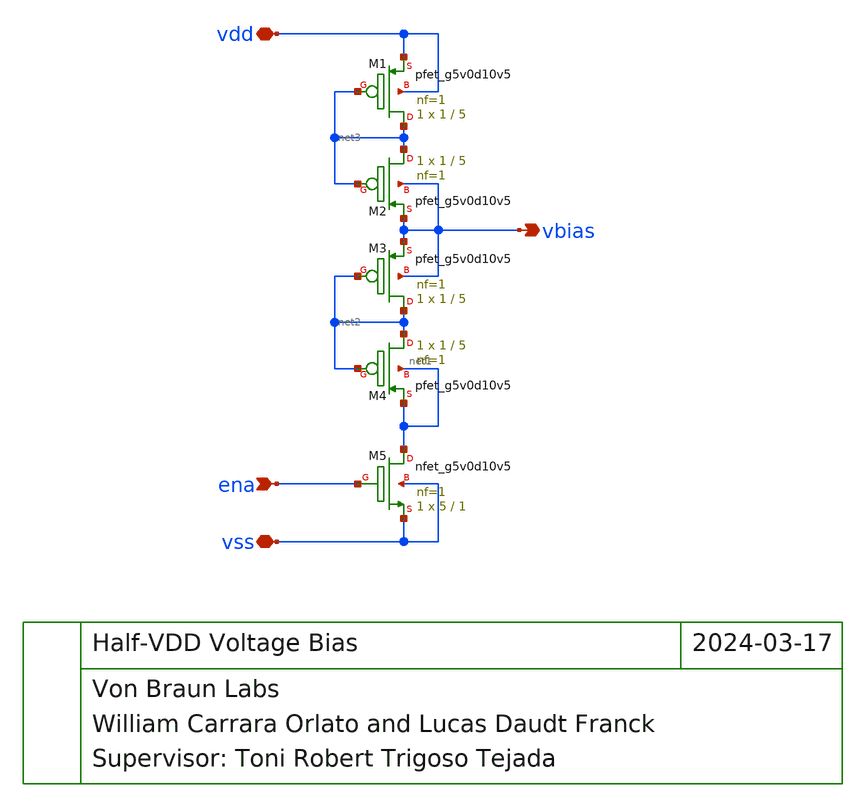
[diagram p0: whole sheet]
** sch_path: xschem_final/halfvdd_vbias.sch
**.subckt halfvdd_vbias ena vss vdd vbias
*.ipin ena
*.iopin vss
*.iopin vdd
*.opin vbias
XM1 net3 net3 vdd vdd sky130_fd_pr__pfet_g5v0d10v5 L=5 W=1 nf=1 ad='int((nf+1)/2) * W/nf * 0.29' as='int((nf+2)/2) * W/nf * 0.29'
+ pd='2*int((nf+1)/2) * (W/nf + 0.29)' ps='2*int((nf+2)/2) * (W/nf + 0.29)' nrd='0.29 / W' nrs='0.29 / W'
+ sa=0 sb=0 sd=0 mult=1 m=1
XM2 net3 net3 vbias vbias sky130_fd_pr__pfet_g5v0d10v5 L=5 W=1 nf=1 ad='int((nf+1)/2) * W/nf * 0.29'
+ as='int((nf+2)/2) * W/nf * 0.29' pd='2*int((nf+1)/2) * (W/nf + 0.29)' ps='2*int((nf+2)/2) * (W/nf + 0.29)'
+ nrd='0.29 / W' nrs='0.29 / W' sa=0 sb=0 sd=0 mult=1 m=1
XM3 net2 net2 vbias vbias sky130_fd_pr__pfet_g5v0d10v5 L=5 W=1 nf=1 ad='int((nf+1)/2) * W/nf * 0.29'
+ as='int((nf+2)/2) * W/nf * 0.29' pd='2*int((nf+1)/2) * (W/nf + 0.29)' ps='2*int((nf+2)/2) * (W/nf + 0.29)'
+ nrd='0.29 / W' nrs='0.29 / W' sa=0 sb=0 sd=0 mult=1 m=1
XM4 net2 net2 net1 net1 sky130_fd_pr__pfet_g5v0d10v5 L=5 W=1 nf=1 ad='int((nf+1)/2) * W/nf * 0.29' as='int((nf+2)/2) * W/nf * 0.29'
+ pd='2*int((nf+1)/2) * (W/nf + 0.29)' ps='2*int((nf+2)/2) * (W/nf + 0.29)' nrd='0.29 / W' nrs='0.29 / W'
+ sa=0 sb=0 sd=0 mult=1 m=1
XM5 net1 ena vss vss sky130_fd_pr__nfet_g5v0d10v5 L=1 W=5 nf=1 ad='int((nf+1)/2) * W/nf * 0.29' as='int((nf+2)/2) * W/nf * 0.29'
+ pd='2*int((nf+1)/2) * (W/nf + 0.29)' ps='2*int((nf+2)/2) * (W/nf + 0.29)' nrd='0.29 / W' nrs='0.29 / W'
+ sa=0 sb=0 sd=0 mult=1 m=1
**.ends
.end
